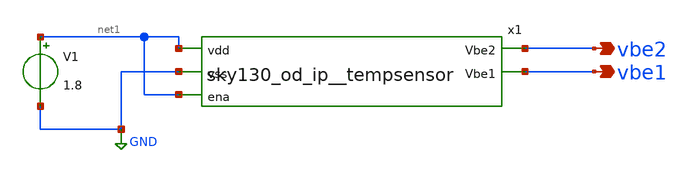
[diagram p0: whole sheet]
** sch_path: xschem/sky130_od_ip__tempsensor_tb.sch
**.subckt sky130_od_ip__tempsensor_tb vbe2 vbe1
*.opin vbe2
*.opin vbe1
V1 net1 GND 1.8
x1 net1 GND vbe2 vbe1 net1 sky130_od_ip__tempsensor
**** begin user architecture code

.lib /usr/local/share/pdk/sky130A/libs.tech/ngspice/sky130.lib.spice tt



.func mu(vbe1,vbe2) = 8.5252/(8.5252+vbe1/(vbe2-vbe1))
.func T(mu) = 802.143*mu-255.537
.control
option TEMP=25
op
let ttrim = T(mu(V(vbe1),V(vbe2)))-25
*let ttrim=0
*print ttrim
*** DEBUG - search for linear mode trasistor
set altshow
show > /tmp/tras.txt

dc temp -40 125 10
plot V(vbe1) V(vbe2)-V(vbe1) V(vbe1)+9.6325*(V(vbe2)-V(vbe1))
plot T(mu(V(vbe1),V(vbe2)))-op1.ttrim
plot T(mu(V(vbe1),V(vbe2)))-"temp-sweep"-op1.ttrim
plot V(vbe1) V(vbe2)


.endc

**** end user architecture code
**.ends

* expanding   symbol:  xschem/sky130_od_ip__tempsensor.sym # of pins=5
** sym_path: xschem/sky130_od_ip__tempsensor.sym
** sch_path: xschem/sky130_od_ip__tempsensor.sch
.subckt sky130_od_ip__tempsensor vdd vss Vbe2 Vbe1 ena
*.ipin vdd
*.ipin vss
*.opin Vbe2
*.opin Vbe1
*.ipin ena
XM12 net1 Vp vdd vdd sky130_fd_pr__pfet_01v8 L=1.2 W=1 nf=1 ad='int((nf+1)/2) * W/nf * 0.29' as='int((nf+2)/2) * W/nf * 0.29'
+ pd='2*int((nf+1)/2) * (W/nf + 0.29)' ps='2*int((nf+2)/2) * (W/nf + 0.29)' nrd='0.29 / W' nrs='0.29 / W'
+ sa=0 sb=0 sd=0 mult=5 m=5
XM13 net2 Vp vdd vdd sky130_fd_pr__pfet_01v8 L=1.2 W=1 nf=1 ad='int((nf+1)/2) * W/nf * 0.29' as='int((nf+2)/2) * W/nf * 0.29'
+ pd='2*int((nf+1)/2) * (W/nf + 0.29)' ps='2*int((nf+2)/2) * (W/nf + 0.29)' nrd='0.29 / W' nrs='0.29 / W'
+ sa=0 sb=0 sd=0 mult=1 m=1
XQ_BR vss net3 net1 sky130_fd_pr__pnp_05v5_W3p40L3p40 m=1
XQ_BL vss vss net4 sky130_fd_pr__pnp_05v5_W3p40L3p40 m=1
Rb net2 net4 5k m=1
Rb_5 net3 vss 1k m=1
XM11 net5 Vp vdd vdd sky130_fd_pr__pfet_01v8 L=1.2 W=1 nf=1 ad='int((nf+1)/2) * W/nf * 0.29' as='int((nf+2)/2) * W/nf * 0.29'
+ pd='2*int((nf+1)/2) * (W/nf + 0.29)' ps='2*int((nf+2)/2) * (W/nf + 0.29)' nrd='0.29 / W' nrs='0.29 / W'
+ sa=0 sb=0 sd=0 mult=2 m=2
XM6 net6 net2 net5 net5 sky130_fd_pr__pfet_01v8 L=1.2 W=10 nf=1 ad='int((nf+1)/2) * W/nf * 0.29' as='int((nf+2)/2) * W/nf * 0.29'
+ pd='2*int((nf+1)/2) * (W/nf + 0.29)' ps='2*int((nf+2)/2) * (W/nf + 0.29)' nrd='0.29 / W' nrs='0.29 / W'
+ sa=0 sb=0 sd=0 mult=1 m=1
XM5 net7 net1 net5 net5 sky130_fd_pr__pfet_01v8 L=1.2 W=10 nf=1 ad='int((nf+1)/2) * W/nf * 0.29' as='int((nf+2)/2) * W/nf * 0.29'
+ pd='2*int((nf+1)/2) * (W/nf + 0.29)' ps='2*int((nf+2)/2) * (W/nf + 0.29)' nrd='0.29 / W' nrs='0.29 / W'
+ sa=0 sb=0 sd=0 mult=1 m=1
XM2 net6 net7 vss vss sky130_fd_pr__nfet_01v8 L=1.2 W=10 nf=1 ad='int((nf+1)/2) * W/nf * 0.29' as='int((nf+2)/2) * W/nf * 0.29'
+ pd='2*int((nf+1)/2) * (W/nf + 0.29)' ps='2*int((nf+2)/2) * (W/nf + 0.29)' nrd='0.29 / W' nrs='0.29 / W'
+ sa=0 sb=0 sd=0 mult=1 m=1
XM1 net7 net7 vss vss sky130_fd_pr__nfet_01v8 L=1.2 W=10 nf=1 ad='int((nf+1)/2) * W/nf * 0.29' as='int((nf+2)/2) * W/nf * 0.29'
+ pd='2*int((nf+1)/2) * (W/nf + 0.29)' ps='2*int((nf+2)/2) * (W/nf + 0.29)' nrd='0.29 / W' nrs='0.29 / W'
+ sa=0 sb=0 sd=0 mult=1 m=1
XM9 net8 Vp vdd vdd sky130_fd_pr__pfet_01v8 L=1.2 W=1 nf=1 ad='int((nf+1)/2) * W/nf * 0.29' as='int((nf+2)/2) * W/nf * 0.29'
+ pd='2*int((nf+1)/2) * (W/nf + 0.29)' ps='2*int((nf+2)/2) * (W/nf + 0.29)' nrd='0.29 / W' nrs='0.29 / W'
+ sa=0 sb=0 sd=0 mult=1 m=1
XM10 Vp Vp vdd vdd sky130_fd_pr__pfet_01v8 L=1.2 W=1 nf=1 ad='int((nf+1)/2) * W/nf * 0.29' as='int((nf+2)/2) * W/nf * 0.29'
+ pd='2*int((nf+1)/2) * (W/nf + 0.29)' ps='2*int((nf+2)/2) * (W/nf + 0.29)' nrd='0.29 / W' nrs='0.29 / W'
+ sa=0 sb=0 sd=0 mult=4 m=4
XM7 Vp net8 net10 net10 sky130_fd_pr__nfet_01v8 L=1.2 W=10 nf=1 ad='int((nf+1)/2) * W/nf * 0.29' as='int((nf+2)/2) * W/nf * 0.29'
+ pd='2*int((nf+1)/2) * (W/nf + 0.29)' ps='2*int((nf+2)/2) * (W/nf + 0.29)' nrd='0.29 / W' nrs='0.29 / W'
+ sa=0 sb=0 sd=0 mult=1 m=1
XM8 net8 net8 net9 net9 sky130_fd_pr__nfet_01v8 L=1.2 W=10 nf=1 ad='int((nf+1)/2) * W/nf * 0.29' as='int((nf+2)/2) * W/nf * 0.29'
+ pd='2*int((nf+1)/2) * (W/nf + 0.29)' ps='2*int((nf+2)/2) * (W/nf + 0.29)' nrd='0.29 / W' nrs='0.29 / W'
+ sa=0 sb=0 sd=0 mult=1 m=1
XM3 net10 net6 vss vss sky130_fd_pr__nfet_01v8 L=1.2 W=10 nf=1 ad='int((nf+1)/2) * W/nf * 0.29' as='int((nf+2)/2) * W/nf * 0.29'
+ pd='2*int((nf+1)/2) * (W/nf + 0.29)' ps='2*int((nf+2)/2) * (W/nf + 0.29)' nrd='0.29 / W' nrs='0.29 / W'
+ sa=0 sb=0 sd=0 mult=4 m=4
XM4 net9 net9 vss vss sky130_fd_pr__nfet_01v8 L=1.2 W=1 nf=1 ad='int((nf+1)/2) * W/nf * 0.29' as='int((nf+2)/2) * W/nf * 0.29'
+ pd='2*int((nf+1)/2) * (W/nf + 0.29)' ps='2*int((nf+2)/2) * (W/nf + 0.29)' nrd='0.29 / W' nrs='0.29 / W'
+ sa=0 sb=0 sd=0 mult=20 m=20
XQ_BL1 vss vss Vbe1 sky130_fd_pr__pnp_05v5_W3p40L3p40 m=1
XQ_BR1 vss vss Vbe2 sky130_fd_pr__pnp_05v5_W3p40L3p40 m=1
XM14 Vbe1 Vp vdd vdd sky130_fd_pr__pfet_01v8 L=1.2 W=1 nf=1 ad='int((nf+1)/2) * W/nf * 0.29' as='int((nf+2)/2) * W/nf * 0.29'
+ pd='2*int((nf+1)/2) * (W/nf + 0.29)' ps='2*int((nf+2)/2) * (W/nf + 0.29)' nrd='0.29 / W' nrs='0.29 / W'
+ sa=0 sb=0 sd=0 mult=1 m=1
XM15 Vbe2 Vp vdd vdd sky130_fd_pr__pfet_01v8 L=1.2 W=1 nf=1 ad='int((nf+1)/2) * W/nf * 0.29' as='int((nf+2)/2) * W/nf * 0.29'
+ pd='2*int((nf+1)/2) * (W/nf + 0.29)' ps='2*int((nf+2)/2) * (W/nf + 0.29)' nrd='0.29 / W' nrs='0.29 / W'
+ sa=0 sb=0 sd=0 mult=5 m=5
XM16 Vp ena vdd vdd sky130_fd_pr__pfet_01v8 L=1.2 W=10 nf=1 ad='int((nf+1)/2) * W/nf * 0.29' as='int((nf+2)/2) * W/nf * 0.29'
+ pd='2*int((nf+1)/2) * (W/nf + 0.29)' ps='2*int((nf+2)/2) * (W/nf + 0.29)' nrd='0.29 / W' nrs='0.29 / W'
+ sa=0 sb=0 sd=0 mult=1 m=1
.ends

.GLOBAL GND
.end
